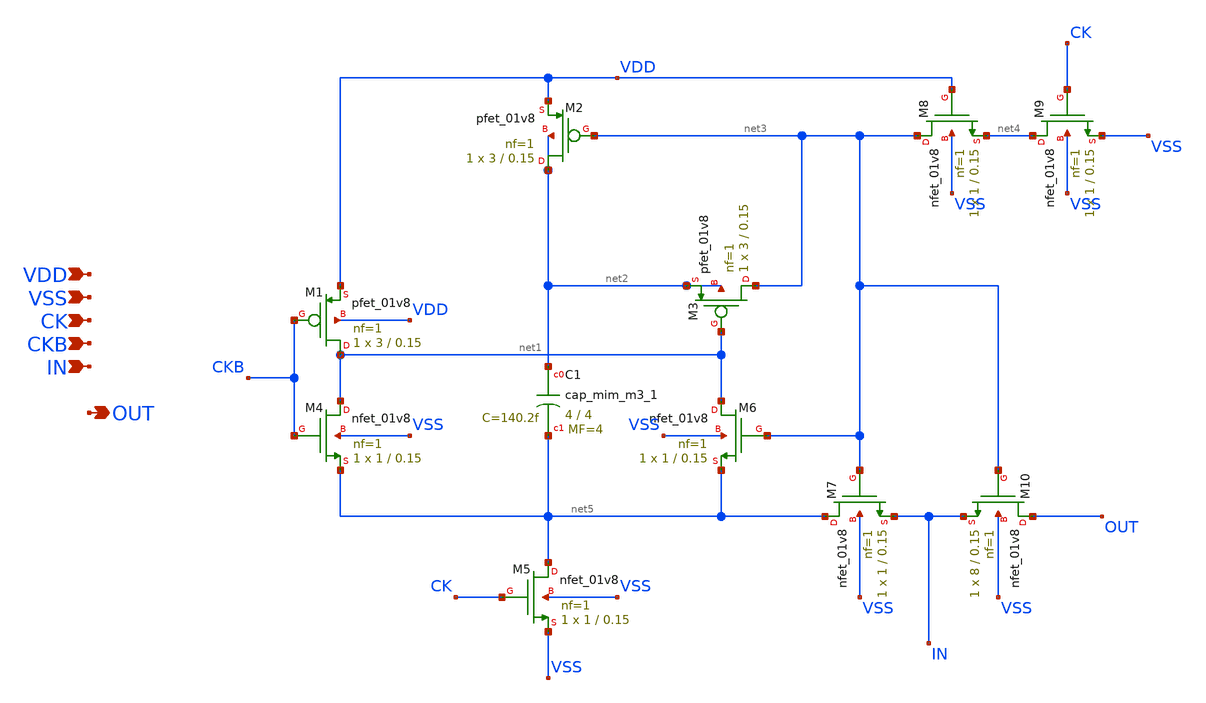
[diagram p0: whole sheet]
** sch_path: xschem/th_sw.sch
**.subckt th_sw VDD VSS CK CKB IN OUT
*.ipin VDD
*.ipin VSS
*.ipin CK
*.ipin CKB
*.ipin IN
*.opin OUT
XM1 net1 CKB VDD VDD sky130_fd_pr__pfet_01v8 L=0.15 W=3 nf=1 ad='int((nf+1)/2) * W/nf * 0.29' as='int((nf+2)/2) * W/nf * 0.29'
+ pd='2*int((nf+1)/2) * (W/nf + 0.29)' ps='2*int((nf+2)/2) * (W/nf + 0.29)' nrd='0.29 / W' nrs='0.29 / W'
+ sa=0 sb=0 sd=0 mult=1 m=1
XM2 net2 net3 VDD net2 sky130_fd_pr__pfet_01v8 L=0.15 W=3 nf=1 ad='int((nf+1)/2) * W/nf * 0.29' as='int((nf+2)/2) * W/nf * 0.29'
+ pd='2*int((nf+1)/2) * (W/nf + 0.29)' ps='2*int((nf+2)/2) * (W/nf + 0.29)' nrd='0.29 / W' nrs='0.29 / W'
+ sa=0 sb=0 sd=0 mult=1 m=1
XM3 net3 net1 net2 net2 sky130_fd_pr__pfet_01v8 L=0.15 W=3 nf=1 ad='int((nf+1)/2) * W/nf * 0.29' as='int((nf+2)/2) * W/nf * 0.29'
+ pd='2*int((nf+1)/2) * (W/nf + 0.29)' ps='2*int((nf+2)/2) * (W/nf + 0.29)' nrd='0.29 / W' nrs='0.29 / W'
+ sa=0 sb=0 sd=0 mult=1 m=1
XM4 net1 CKB net5 VSS sky130_fd_pr__nfet_01v8 L=0.15 W=1 nf=1 ad='int((nf+1)/2) * W/nf * 0.29' as='int((nf+2)/2) * W/nf * 0.29'
+ pd='2*int((nf+1)/2) * (W/nf + 0.29)' ps='2*int((nf+2)/2) * (W/nf + 0.29)' nrd='0.29 / W' nrs='0.29 / W'
+ sa=0 sb=0 sd=0 mult=1 m=1
XM5 net5 CK VSS VSS sky130_fd_pr__nfet_01v8 L=0.15 W=1 nf=1 ad='int((nf+1)/2) * W/nf * 0.29' as='int((nf+2)/2) * W/nf * 0.29'
+ pd='2*int((nf+1)/2) * (W/nf + 0.29)' ps='2*int((nf+2)/2) * (W/nf + 0.29)' nrd='0.29 / W' nrs='0.29 / W'
+ sa=0 sb=0 sd=0 mult=1 m=1
XM6 net1 net3 net5 VSS sky130_fd_pr__nfet_01v8 L=0.15 W=1 nf=1 ad='int((nf+1)/2) * W/nf * 0.29' as='int((nf+2)/2) * W/nf * 0.29'
+ pd='2*int((nf+1)/2) * (W/nf + 0.29)' ps='2*int((nf+2)/2) * (W/nf + 0.29)' nrd='0.29 / W' nrs='0.29 / W'
+ sa=0 sb=0 sd=0 mult=1 m=1
XM7 net5 net3 IN VSS sky130_fd_pr__nfet_01v8 L=0.15 W=1 nf=1 ad='int((nf+1)/2) * W/nf * 0.29' as='int((nf+2)/2) * W/nf * 0.29'
+ pd='2*int((nf+1)/2) * (W/nf + 0.29)' ps='2*int((nf+2)/2) * (W/nf + 0.29)' nrd='0.29 / W' nrs='0.29 / W'
+ sa=0 sb=0 sd=0 mult=1 m=1
XM8 net3 VDD net4 VSS sky130_fd_pr__nfet_01v8 L=0.15 W=1 nf=1 ad='int((nf+1)/2) * W/nf * 0.29' as='int((nf+2)/2) * W/nf * 0.29'
+ pd='2*int((nf+1)/2) * (W/nf + 0.29)' ps='2*int((nf+2)/2) * (W/nf + 0.29)' nrd='0.29 / W' nrs='0.29 / W'
+ sa=0 sb=0 sd=0 mult=1 m=1
XM9 net4 CK VSS VSS sky130_fd_pr__nfet_01v8 L=0.15 W=1 nf=1 ad='int((nf+1)/2) * W/nf * 0.29' as='int((nf+2)/2) * W/nf * 0.29'
+ pd='2*int((nf+1)/2) * (W/nf + 0.29)' ps='2*int((nf+2)/2) * (W/nf + 0.29)' nrd='0.29 / W' nrs='0.29 / W'
+ sa=0 sb=0 sd=0 mult=1 m=1
XC1 net2 net5 sky130_fd_pr__cap_mim_m3_1 W=4 L=4 MF=4 m=4
XM10 OUT net3 IN VSS sky130_fd_pr__nfet_01v8 L=0.15 W=8 nf=1 ad='int((nf+1)/2) * W/nf * 0.29' as='int((nf+2)/2) * W/nf * 0.29'
+ pd='2*int((nf+1)/2) * (W/nf + 0.29)' ps='2*int((nf+2)/2) * (W/nf + 0.29)' nrd='0.29 / W' nrs='0.29 / W'
+ sa=0 sb=0 sd=0 mult=1 m=1
**.ends
.end
